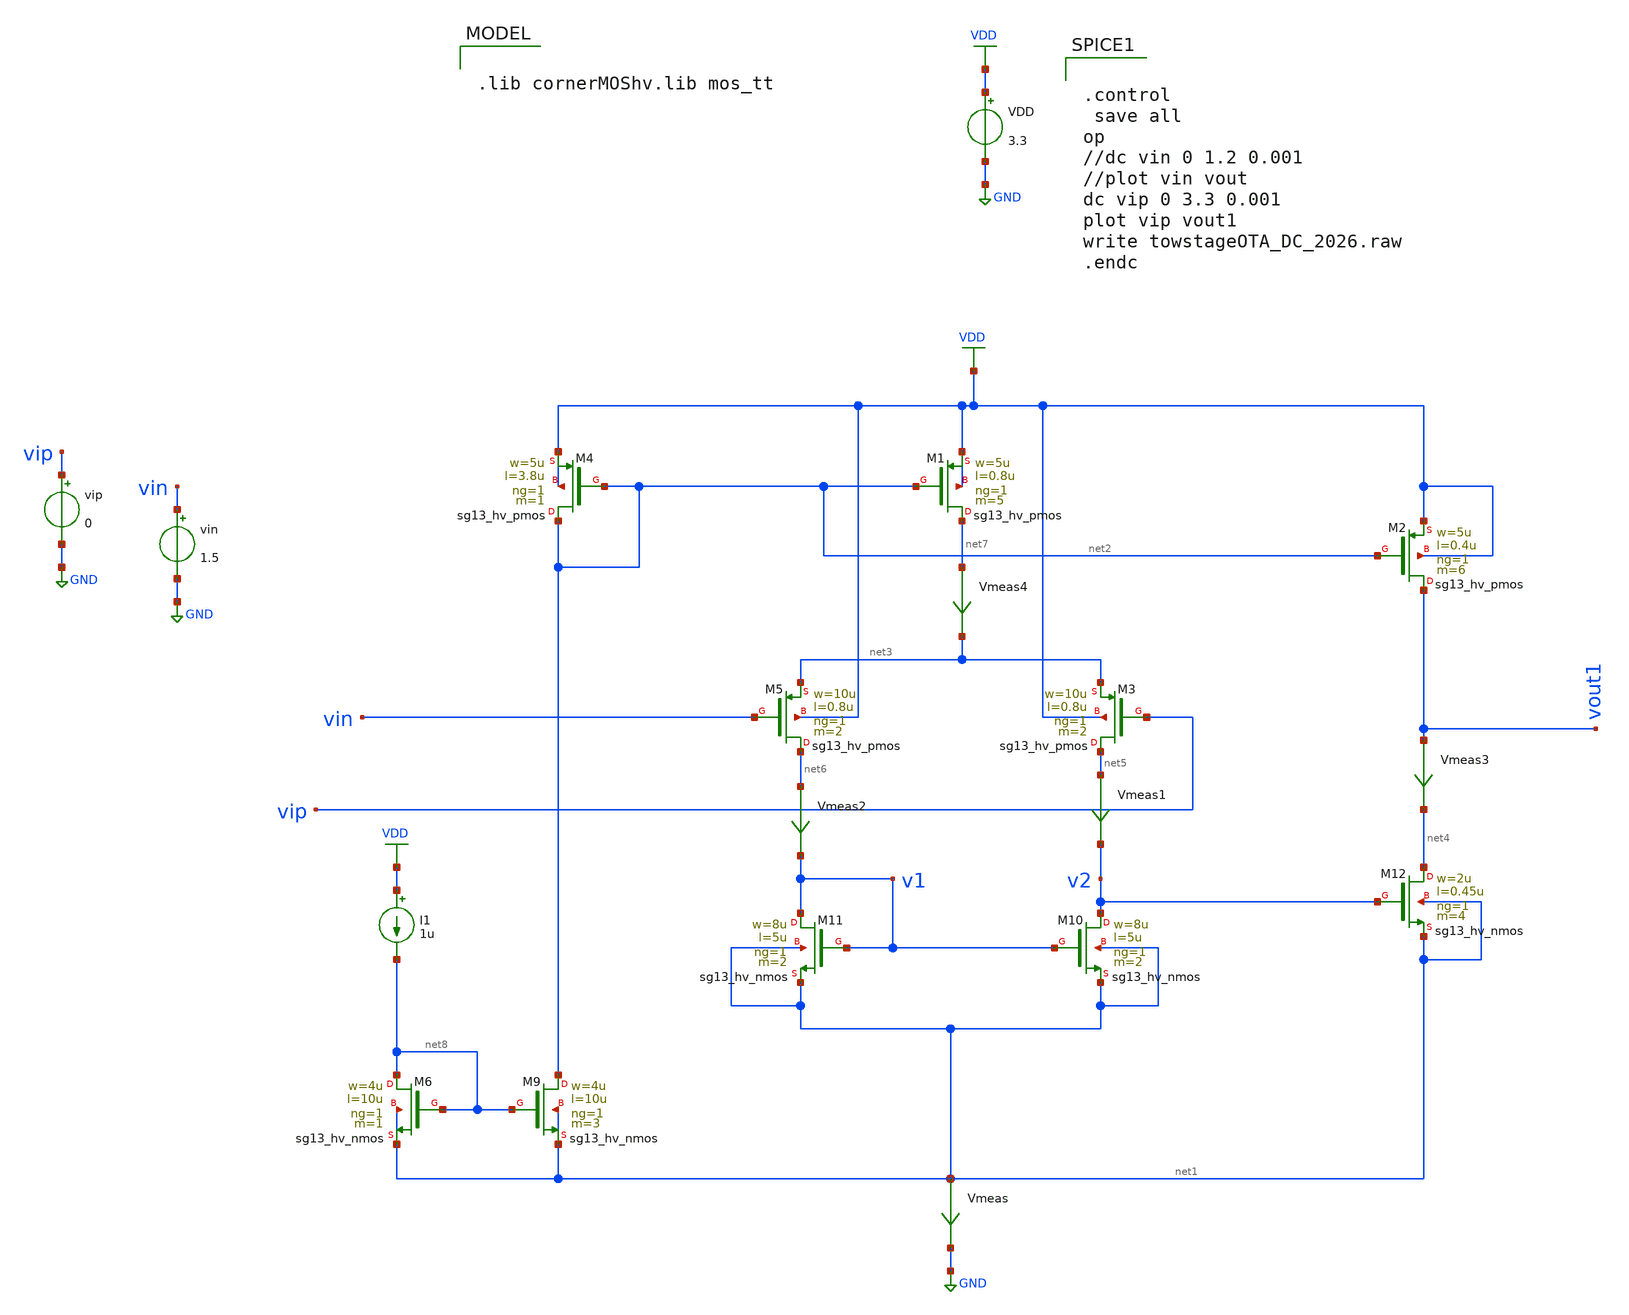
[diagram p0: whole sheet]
** sch_path: dependencies/ClockExtractor/ClockExtractor-main/schematic/xschem/schematic/TowStageOTA_DC_2026.sch
**.subckt TowStageOTA_DC_2026
VDD VDD GND 3.3
XM4 net2 net2 VDD VDD sg13_hv_pmos w=5u l=3.8u ng=1 m=1 mm_ok=1
XM1 net7 net2 VDD VDD sg13_hv_pmos w=5u l=0.8u ng=1 m=5 mm_ok=1
XM2 vout1 net2 VDD VDD sg13_hv_pmos w=5u l=0.4u ng=1 m=6 mm_ok=1
XM3 net5 vip net3 VDD sg13_hv_pmos w=10u l=0.8u ng=1 m=2 mm_ok=1
XM5 net6 vin net3 VDD sg13_hv_pmos w=10u l=0.8u ng=1 m=2 mm_ok=1
XM10 v2 v1 net1 net1 sg13_hv_nmos w=8u l=5u ng=1 m=2 mm_ok=1
XM11 v1 v1 net1 net1 sg13_hv_nmos w=8u l=5u ng=1 m=2 mm_ok=1
XM12 net4 v2 net1 net1 sg13_hv_nmos w=2u l=0.45u ng=1 m=4 mm_ok=1
vin vin GND 1.5
vip vip GND 0
Vmeas net1 GND 0
.save i(vmeas)
Vmeas1 net5 v2 0
.save i(vmeas1)
Vmeas2 net6 v1 0
.save i(vmeas2)
Vmeas3 vout1 net4 0
.save i(vmeas3)
Vmeas4 net7 net3 0
.save i(vmeas4)
I1 VDD net8 1u
XM9 net2 net8 net1 net1 sg13_hv_nmos w=4u l=10u ng=1 m=3 mm_ok=1
XM6 net8 net8 net1 net1 sg13_hv_nmos w=4u l=10u ng=1 m=1 mm_ok=1
**** begin user architecture code

.lib cornerMOShv.lib mos_tt



.control
 save all
op
//dc vin 0 1.2 0.001
//plot vin vout
dc vip 0 3.3 0.001
plot vip vout1
write towstageOTA_DC_2026.raw
.endc


**** end user architecture code
**.ends
.GLOBAL GND
.GLOBAL VDD
.end
